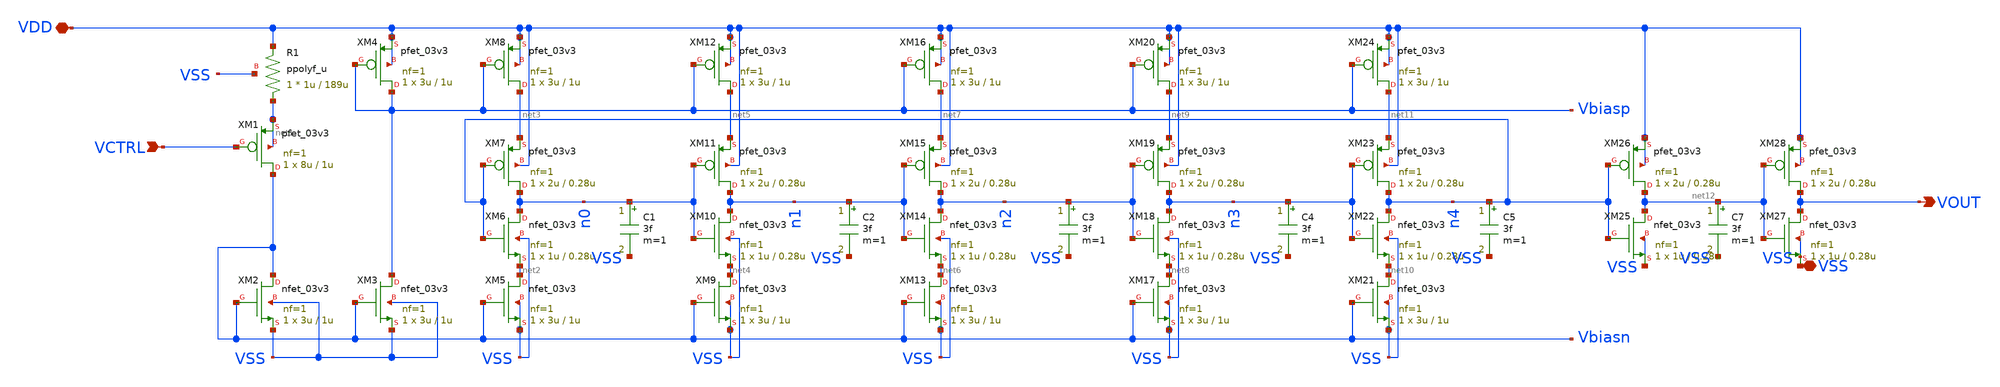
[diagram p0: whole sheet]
** sch_path: analog/vco/vco.sch
**.subckt vco VCTRL VDD VOUT VSS
*.ipin VCTRL
*.iopin VDD
*.opin VOUT
*.iopin VSS
XM1 Vbiasn VCTRL net1 net1 pfet_03v3 L=1u W=8u nf=1 ad='int((nf+1)/2) * W/nf * 0.18u' as='int((nf+2)/2) * W/nf * 0.18u'
+ pd='2*int((nf+1)/2) * (W/nf + 0.18u)' ps='2*int((nf+2)/2) * (W/nf + 0.18u)' nrd='0.18u / W' nrs='0.18u / W'
+ sa=0 sb=0 sd=0 m=1
XM2 Vbiasn Vbiasn VSS VSS nfet_03v3 L=1u W=3u nf=1 ad='int((nf+1)/2) * W/nf * 0.18u' as='int((nf+2)/2) * W/nf * 0.18u'
+ pd='2*int((nf+1)/2) * (W/nf + 0.18u)' ps='2*int((nf+2)/2) * (W/nf + 0.18u)' nrd='0.18u / W' nrs='0.18u / W'
+ sa=0 sb=0 sd=0 m=1
XM3 Vbiasp Vbiasn VSS VSS nfet_03v3 L=1u W=3u nf=1 ad='int((nf+1)/2) * W/nf * 0.18u' as='int((nf+2)/2) * W/nf * 0.18u'
+ pd='2*int((nf+1)/2) * (W/nf + 0.18u)' ps='2*int((nf+2)/2) * (W/nf + 0.18u)' nrd='0.18u / W' nrs='0.18u / W'
+ sa=0 sb=0 sd=0 m=1
XM4 Vbiasp Vbiasp VDD VDD pfet_03v3 L=1u W=3u nf=1 ad='int((nf+1)/2) * W/nf * 0.18u' as='int((nf+2)/2) * W/nf * 0.18u'
+ pd='2*int((nf+1)/2) * (W/nf + 0.18u)' ps='2*int((nf+2)/2) * (W/nf + 0.18u)' nrd='0.18u / W' nrs='0.18u / W'
+ sa=0 sb=0 sd=0 m=1
XR1 net1 VDD VSS ppolyf_u r_width=1u r_length=189u m=1
XM5 net2 Vbiasn VSS VSS nfet_03v3 L=1u W=3u nf=1 ad='int((nf+1)/2) * W/nf * 0.18u' as='int((nf+2)/2) * W/nf * 0.18u'
+ pd='2*int((nf+1)/2) * (W/nf + 0.18u)' ps='2*int((nf+2)/2) * (W/nf + 0.18u)' nrd='0.18u / W' nrs='0.18u / W'
+ sa=0 sb=0 sd=0 m=1
XM6 n0 n4 net2 VSS nfet_03v3 L=0.28u W=1u nf=1 ad='int((nf+1)/2) * W/nf * 0.18u' as='int((nf+2)/2) * W/nf * 0.18u'
+ pd='2*int((nf+1)/2) * (W/nf + 0.18u)' ps='2*int((nf+2)/2) * (W/nf + 0.18u)' nrd='0.18u / W' nrs='0.18u / W'
+ sa=0 sb=0 sd=0 m=1
XM7 n0 n4 net3 VDD pfet_03v3 L=0.28u W=2u nf=1 ad='int((nf+1)/2) * W/nf * 0.18u' as='int((nf+2)/2) * W/nf * 0.18u'
+ pd='2*int((nf+1)/2) * (W/nf + 0.18u)' ps='2*int((nf+2)/2) * (W/nf + 0.18u)' nrd='0.18u / W' nrs='0.18u / W'
+ sa=0 sb=0 sd=0 m=1
XM8 net3 Vbiasp VDD VDD pfet_03v3 L=1u W=3u nf=1 ad='int((nf+1)/2) * W/nf * 0.18u' as='int((nf+2)/2) * W/nf * 0.18u'
+ pd='2*int((nf+1)/2) * (W/nf + 0.18u)' ps='2*int((nf+2)/2) * (W/nf + 0.18u)' nrd='0.18u / W' nrs='0.18u / W'
+ sa=0 sb=0 sd=0 m=1
XM9 net4 Vbiasn VSS VSS nfet_03v3 L=1u W=3u nf=1 ad='int((nf+1)/2) * W/nf * 0.18u' as='int((nf+2)/2) * W/nf * 0.18u'
+ pd='2*int((nf+1)/2) * (W/nf + 0.18u)' ps='2*int((nf+2)/2) * (W/nf + 0.18u)' nrd='0.18u / W' nrs='0.18u / W'
+ sa=0 sb=0 sd=0 m=1
XM10 n1 n0 net4 VSS nfet_03v3 L=0.28u W=1u nf=1 ad='int((nf+1)/2) * W/nf * 0.18u' as='int((nf+2)/2) * W/nf * 0.18u'
+ pd='2*int((nf+1)/2) * (W/nf + 0.18u)' ps='2*int((nf+2)/2) * (W/nf + 0.18u)' nrd='0.18u / W' nrs='0.18u / W'
+ sa=0 sb=0 sd=0 m=1
XM11 n1 n0 net5 VDD pfet_03v3 L=0.28u W=2u nf=1 ad='int((nf+1)/2) * W/nf * 0.18u' as='int((nf+2)/2) * W/nf * 0.18u'
+ pd='2*int((nf+1)/2) * (W/nf + 0.18u)' ps='2*int((nf+2)/2) * (W/nf + 0.18u)' nrd='0.18u / W' nrs='0.18u / W'
+ sa=0 sb=0 sd=0 m=1
XM12 net5 Vbiasp VDD VDD pfet_03v3 L=1u W=3u nf=1 ad='int((nf+1)/2) * W/nf * 0.18u' as='int((nf+2)/2) * W/nf * 0.18u'
+ pd='2*int((nf+1)/2) * (W/nf + 0.18u)' ps='2*int((nf+2)/2) * (W/nf + 0.18u)' nrd='0.18u / W' nrs='0.18u / W'
+ sa=0 sb=0 sd=0 m=1
XM13 net6 Vbiasn VSS VSS nfet_03v3 L=1u W=3u nf=1 ad='int((nf+1)/2) * W/nf * 0.18u' as='int((nf+2)/2) * W/nf * 0.18u'
+ pd='2*int((nf+1)/2) * (W/nf + 0.18u)' ps='2*int((nf+2)/2) * (W/nf + 0.18u)' nrd='0.18u / W' nrs='0.18u / W'
+ sa=0 sb=0 sd=0 m=1
XM14 n2 n1 net6 VSS nfet_03v3 L=0.28u W=1u nf=1 ad='int((nf+1)/2) * W/nf * 0.18u' as='int((nf+2)/2) * W/nf * 0.18u'
+ pd='2*int((nf+1)/2) * (W/nf + 0.18u)' ps='2*int((nf+2)/2) * (W/nf + 0.18u)' nrd='0.18u / W' nrs='0.18u / W'
+ sa=0 sb=0 sd=0 m=1
XM15 n2 n1 net7 VDD pfet_03v3 L=0.28u W=2u nf=1 ad='int((nf+1)/2) * W/nf * 0.18u' as='int((nf+2)/2) * W/nf * 0.18u'
+ pd='2*int((nf+1)/2) * (W/nf + 0.18u)' ps='2*int((nf+2)/2) * (W/nf + 0.18u)' nrd='0.18u / W' nrs='0.18u / W'
+ sa=0 sb=0 sd=0 m=1
XM16 net7 Vbiasp VDD VDD pfet_03v3 L=1u W=3u nf=1 ad='int((nf+1)/2) * W/nf * 0.18u' as='int((nf+2)/2) * W/nf * 0.18u'
+ pd='2*int((nf+1)/2) * (W/nf + 0.18u)' ps='2*int((nf+2)/2) * (W/nf + 0.18u)' nrd='0.18u / W' nrs='0.18u / W'
+ sa=0 sb=0 sd=0 m=1
XM17 net8 Vbiasn VSS VSS nfet_03v3 L=1u W=3u nf=1 ad='int((nf+1)/2) * W/nf * 0.18u' as='int((nf+2)/2) * W/nf * 0.18u'
+ pd='2*int((nf+1)/2) * (W/nf + 0.18u)' ps='2*int((nf+2)/2) * (W/nf + 0.18u)' nrd='0.18u / W' nrs='0.18u / W'
+ sa=0 sb=0 sd=0 m=1
XM18 n3 n2 net8 VSS nfet_03v3 L=0.28u W=1u nf=1 ad='int((nf+1)/2) * W/nf * 0.18u' as='int((nf+2)/2) * W/nf * 0.18u'
+ pd='2*int((nf+1)/2) * (W/nf + 0.18u)' ps='2*int((nf+2)/2) * (W/nf + 0.18u)' nrd='0.18u / W' nrs='0.18u / W'
+ sa=0 sb=0 sd=0 m=1
XM19 n3 n2 net9 VDD pfet_03v3 L=0.28u W=2u nf=1 ad='int((nf+1)/2) * W/nf * 0.18u' as='int((nf+2)/2) * W/nf * 0.18u'
+ pd='2*int((nf+1)/2) * (W/nf + 0.18u)' ps='2*int((nf+2)/2) * (W/nf + 0.18u)' nrd='0.18u / W' nrs='0.18u / W'
+ sa=0 sb=0 sd=0 m=1
XM20 net9 Vbiasp VDD VDD pfet_03v3 L=1u W=3u nf=1 ad='int((nf+1)/2) * W/nf * 0.18u' as='int((nf+2)/2) * W/nf * 0.18u'
+ pd='2*int((nf+1)/2) * (W/nf + 0.18u)' ps='2*int((nf+2)/2) * (W/nf + 0.18u)' nrd='0.18u / W' nrs='0.18u / W'
+ sa=0 sb=0 sd=0 m=1
XM21 net10 Vbiasn VSS VSS nfet_03v3 L=1u W=3u nf=1 ad='int((nf+1)/2) * W/nf * 0.18u' as='int((nf+2)/2) * W/nf * 0.18u'
+ pd='2*int((nf+1)/2) * (W/nf + 0.18u)' ps='2*int((nf+2)/2) * (W/nf + 0.18u)' nrd='0.18u / W' nrs='0.18u / W'
+ sa=0 sb=0 sd=0 m=1
XM22 n4 n3 net10 VSS nfet_03v3 L=0.28u W=1u nf=1 ad='int((nf+1)/2) * W/nf * 0.18u' as='int((nf+2)/2) * W/nf * 0.18u'
+ pd='2*int((nf+1)/2) * (W/nf + 0.18u)' ps='2*int((nf+2)/2) * (W/nf + 0.18u)' nrd='0.18u / W' nrs='0.18u / W'
+ sa=0 sb=0 sd=0 m=1
XM23 n4 n3 net11 VDD pfet_03v3 L=0.28u W=2u nf=1 ad='int((nf+1)/2) * W/nf * 0.18u' as='int((nf+2)/2) * W/nf * 0.18u'
+ pd='2*int((nf+1)/2) * (W/nf + 0.18u)' ps='2*int((nf+2)/2) * (W/nf + 0.18u)' nrd='0.18u / W' nrs='0.18u / W'
+ sa=0 sb=0 sd=0 m=1
XM24 net11 Vbiasp VDD VDD pfet_03v3 L=1u W=3u nf=1 ad='int((nf+1)/2) * W/nf * 0.18u' as='int((nf+2)/2) * W/nf * 0.18u'
+ pd='2*int((nf+1)/2) * (W/nf + 0.18u)' ps='2*int((nf+2)/2) * (W/nf + 0.18u)' nrd='0.18u / W' nrs='0.18u / W'
+ sa=0 sb=0 sd=0 m=1
C1 n0 VSS 3f m=1
C2 n1 VSS 3f m=1
C3 n2 VSS 3f m=1
C4 n3 VSS 3f m=1
C5 n4 VSS 3f m=1
XM25 net12 n4 VSS VSS nfet_03v3 L=0.28u W=1u nf=1 ad='int((nf+1)/2) * W/nf * 0.18u' as='int((nf+2)/2) * W/nf * 0.18u'
+ pd='2*int((nf+1)/2) * (W/nf + 0.18u)' ps='2*int((nf+2)/2) * (W/nf + 0.18u)' nrd='0.18u / W' nrs='0.18u / W'
+ sa=0 sb=0 sd=0 m=1
XM26 net12 n4 VDD VDD pfet_03v3 L=0.28u W=2u nf=1 ad='int((nf+1)/2) * W/nf * 0.18u' as='int((nf+2)/2) * W/nf * 0.18u'
+ pd='2*int((nf+1)/2) * (W/nf + 0.18u)' ps='2*int((nf+2)/2) * (W/nf + 0.18u)' nrd='0.18u / W' nrs='0.18u / W'
+ sa=0 sb=0 sd=0 m=1
XM27 VOUT net12 VSS VSS nfet_03v3 L=0.28u W=1u nf=1 ad='int((nf+1)/2) * W/nf * 0.18u' as='int((nf+2)/2) * W/nf * 0.18u'
+ pd='2*int((nf+1)/2) * (W/nf + 0.18u)' ps='2*int((nf+2)/2) * (W/nf + 0.18u)' nrd='0.18u / W' nrs='0.18u / W'
+ sa=0 sb=0 sd=0 m=1
XM28 VOUT net12 VDD VDD pfet_03v3 L=0.28u W=2u nf=1 ad='int((nf+1)/2) * W/nf * 0.18u' as='int((nf+2)/2) * W/nf * 0.18u'
+ pd='2*int((nf+1)/2) * (W/nf + 0.18u)' ps='2*int((nf+2)/2) * (W/nf + 0.18u)' nrd='0.18u / W' nrs='0.18u / W'
+ sa=0 sb=0 sd=0 m=1
C7 net12 VSS 3f m=1
**.ends
.end
